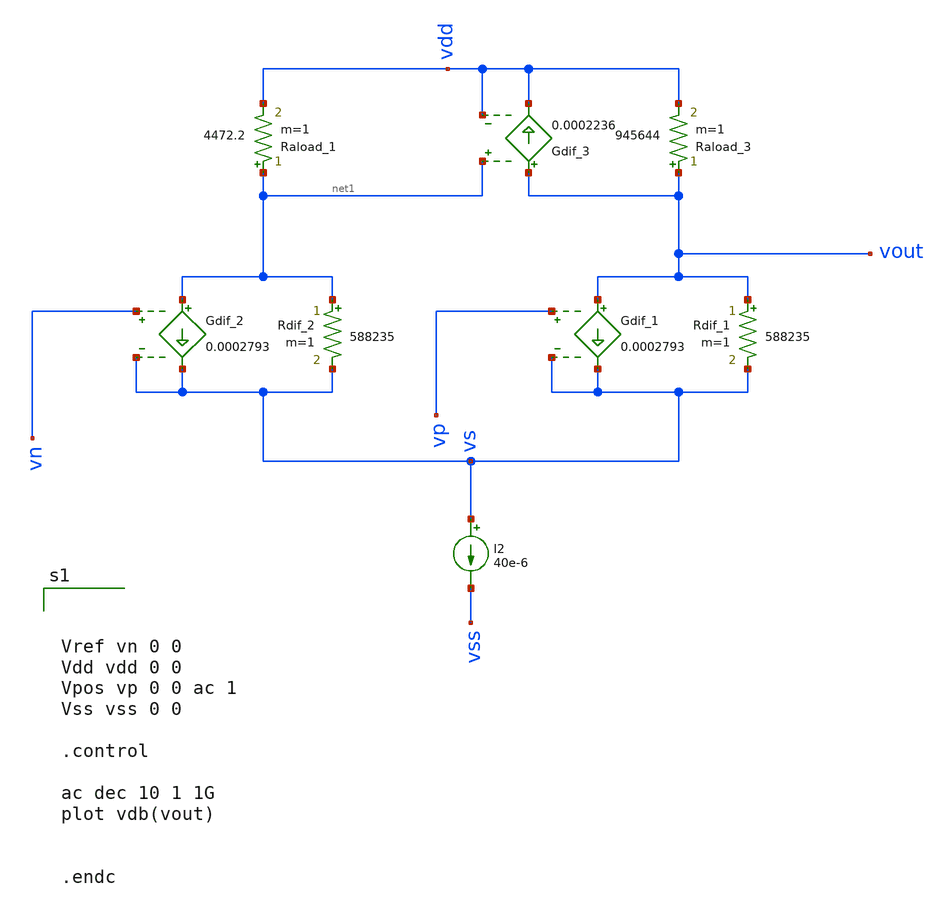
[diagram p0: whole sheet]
** sch_path: test/result_comp/xschem/ota_tb.sch
**.subckt ota_tb
Rdif_2 net1 vs 588235 m=1
Gdif_2 net1 vs vn vs 0.0002793
Rdif_1 vout vs 588235 m=1
Gdif_1 vout vs vp vs 0.0002793
I2 vs vss 40e-6
Raload_3 vout vdd 945644 m=1
Raload_1 net1 vdd 4472.2 m=1
Gdif_3 vout vdd net1 vdd 0.0002236
**** begin user architecture code



Vref vn 0 0
Vdd vdd 0 0
Vpos vp 0 0 ac 1
Vss vss 0 0

.control

ac dec 10 1 1G
plot vdb(vout)


.endc



**** end user architecture code
**.ends
.end
